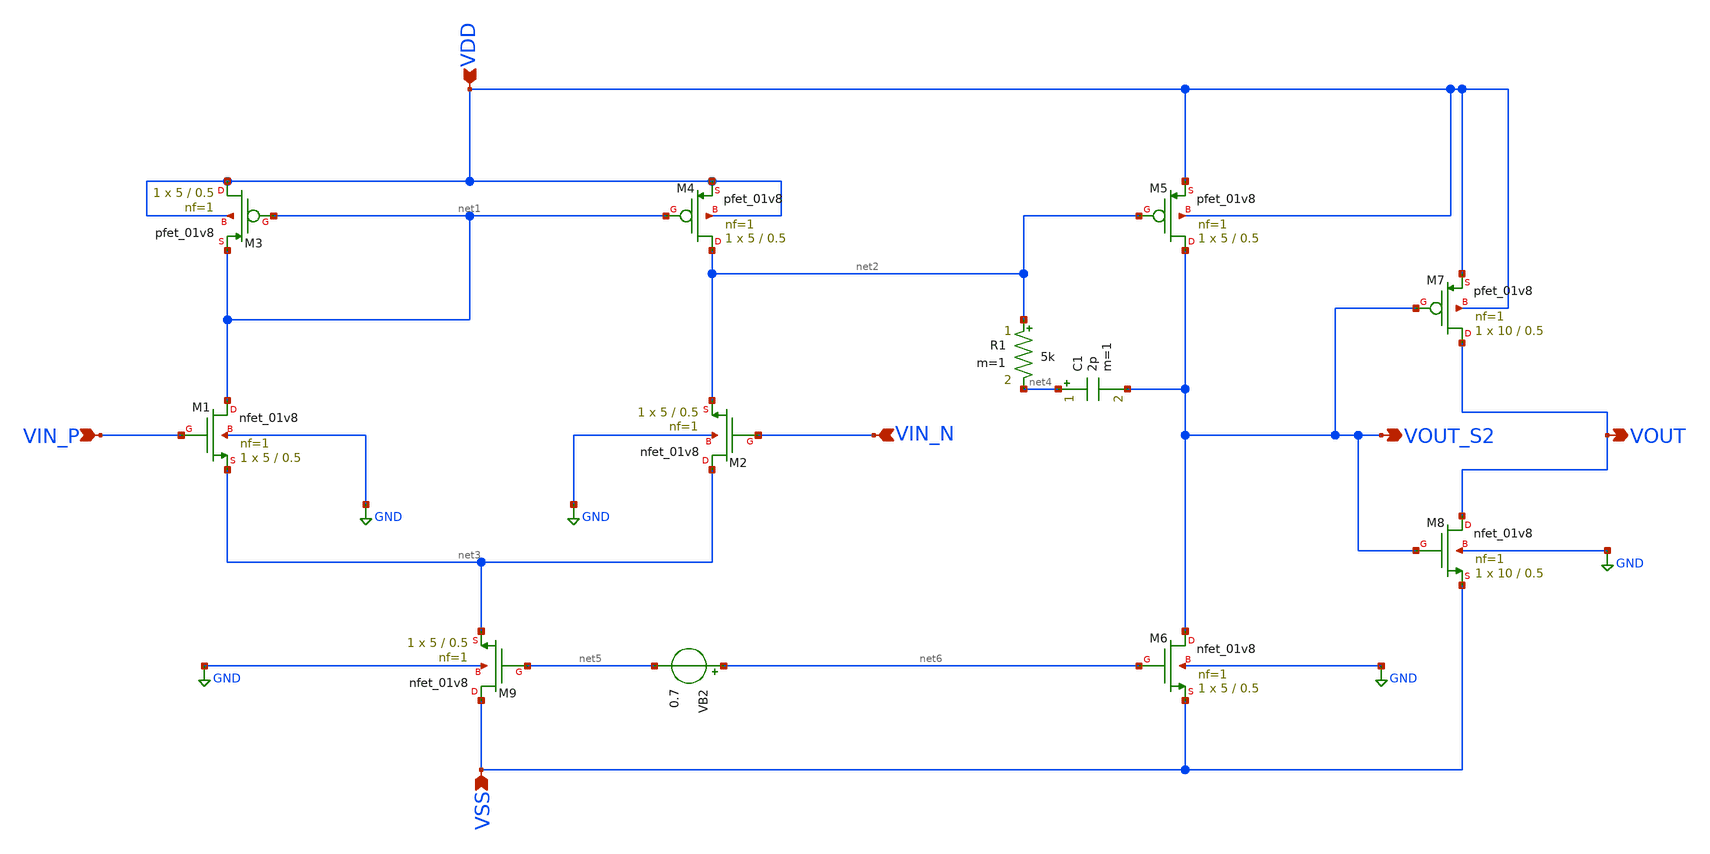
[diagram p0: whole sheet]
** sch_path: analog/schematics/opamp_single_stage.sch
**.subckt opamp_single_stage VIN_P VIN_N VDD VSS VOUT_S2 VOUT
*.ipin VIN_P
*.ipin VIN_N
*.ipin VDD
*.ipin VSS
*.opin VOUT_S2
*.opin VOUT
XM3 VDD net1 net1 VDD sky130_fd_pr__pfet_01v8 L=0.5 W=5 nf=1 ad='int((nf+1)/2) * W/nf * 0.29' as='int((nf+2)/2) * W/nf * 0.29'
+ pd='2*int((nf+1)/2) * (W/nf + 0.29)' ps='2*int((nf+2)/2) * (W/nf + 0.29)' nrd='0.29 / W' nrs='0.29 / W'
+ sa=0 sb=0 sd=0 mult=1 m=1
XM4 net2 net1 VDD VDD sky130_fd_pr__pfet_01v8 L=0.5 W=5 nf=1 ad='int((nf+1)/2) * W/nf * 0.29' as='int((nf+2)/2) * W/nf * 0.29'
+ pd='2*int((nf+1)/2) * (W/nf + 0.29)' ps='2*int((nf+2)/2) * (W/nf + 0.29)' nrd='0.29 / W' nrs='0.29 / W'
+ sa=0 sb=0 sd=0 mult=1 m=1
VB2 net6 net5 0.7
XM1 net1 VIN_P net3 GND sky130_fd_pr__nfet_01v8 L=0.5 W=5 nf=1 ad='int((nf+1)/2) * W/nf * 0.29' as='int((nf+2)/2) * W/nf * 0.29'
+ pd='2*int((nf+1)/2) * (W/nf + 0.29)' ps='2*int((nf+2)/2) * (W/nf + 0.29)' nrd='0.29 / W' nrs='0.29 / W'
+ sa=0 sb=0 sd=0 mult=1 m=1
XM2 net3 VIN_N net2 GND sky130_fd_pr__nfet_01v8 L=0.5 W=5 nf=1 ad='int((nf+1)/2) * W/nf * 0.29' as='int((nf+2)/2) * W/nf * 0.29'
+ pd='2*int((nf+1)/2) * (W/nf + 0.29)' ps='2*int((nf+2)/2) * (W/nf + 0.29)' nrd='0.29 / W' nrs='0.29 / W'
+ sa=0 sb=0 sd=0 mult=1 m=1
XM9 VSS net5 net3 GND sky130_fd_pr__nfet_01v8 L=0.5 W=5 nf=1 ad='int((nf+1)/2) * W/nf * 0.29' as='int((nf+2)/2) * W/nf * 0.29'
+ pd='2*int((nf+1)/2) * (W/nf + 0.29)' ps='2*int((nf+2)/2) * (W/nf + 0.29)' nrd='0.29 / W' nrs='0.29 / W'
+ sa=0 sb=0 sd=0 mult=1 m=1
XM5 VOUT_S2 net2 VDD VDD sky130_fd_pr__pfet_01v8 L=0.5 W=5 nf=1 ad='int((nf+1)/2) * W/nf * 0.29' as='int((nf+2)/2) * W/nf * 0.29'
+ pd='2*int((nf+1)/2) * (W/nf + 0.29)' ps='2*int((nf+2)/2) * (W/nf + 0.29)' nrd='0.29 / W' nrs='0.29 / W'
+ sa=0 sb=0 sd=0 mult=1 m=1
XM6 VOUT_S2 net6 VSS GND sky130_fd_pr__nfet_01v8 L=0.5 W=5 nf=1 ad='int((nf+1)/2) * W/nf * 0.29' as='int((nf+2)/2) * W/nf * 0.29'
+ pd='2*int((nf+1)/2) * (W/nf + 0.29)' ps='2*int((nf+2)/2) * (W/nf + 0.29)' nrd='0.29 / W' nrs='0.29 / W'
+ sa=0 sb=0 sd=0 mult=1 m=1
R1 net2 net4 5k m=1
C1 net4 VOUT_S2 2p m=1
XM7 VOUT VOUT_S2 VDD VDD sky130_fd_pr__pfet_01v8 L=0.5 W=10 nf=1 ad='int((nf+1)/2) * W/nf * 0.29' as='int((nf+2)/2) * W/nf * 0.29'
+ pd='2*int((nf+1)/2) * (W/nf + 0.29)' ps='2*int((nf+2)/2) * (W/nf + 0.29)' nrd='0.29 / W' nrs='0.29 / W'
+ sa=0 sb=0 sd=0 mult=1 m=1
XM8 VOUT VOUT_S2 VSS GND sky130_fd_pr__nfet_01v8 L=0.5 W=10 nf=1 ad='int((nf+1)/2) * W/nf * 0.29' as='int((nf+2)/2) * W/nf * 0.29'
+ pd='2*int((nf+1)/2) * (W/nf + 0.29)' ps='2*int((nf+2)/2) * (W/nf + 0.29)' nrd='0.29 / W' nrs='0.29 / W'
+ sa=0 sb=0 sd=0 mult=1 m=1
**.ends
.GLOBAL GND
.end
